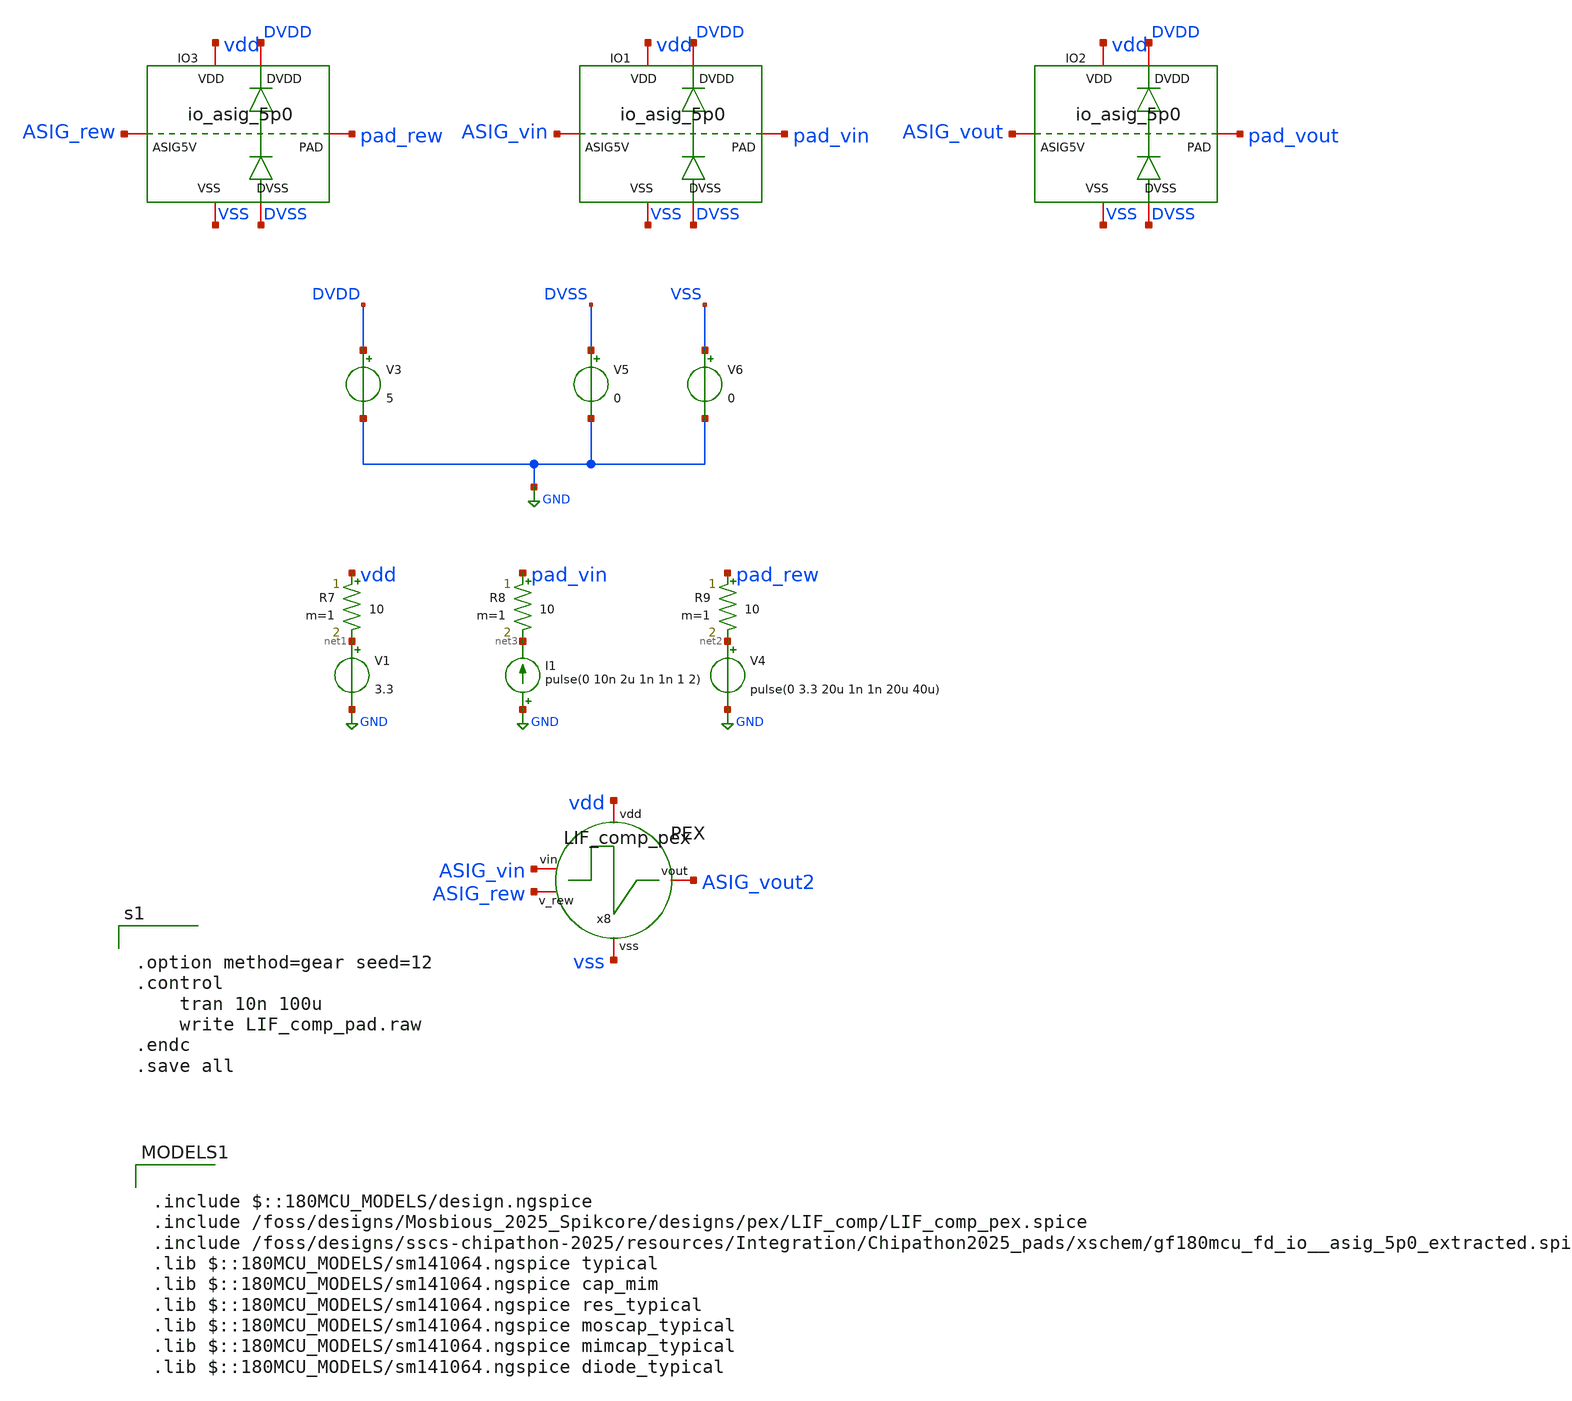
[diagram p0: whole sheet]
** sch_path: designs/pex_PADS/tb_LIF_comp/LIF_comp.sch
**.subckt LIF_comp
V1 net1 GND 3.3
V4 net2 GND pulse(0 3.3 20u 1n 1n 20u 40u)
x8 vdd vss ASIG_vin ASIG_rew ASIG_vout2 LIF_comp_pex
I1 GND net3 pulse(0 10n 2u 1n 1n 1 2)
R7 vdd net1 10 m=1
R8 pad_vin net3 10 m=1
R9 pad_rew net2 10 m=1
V3 DVDD GND 5
V5 DVSS GND 0
V6 VSS GND 0
XIO1 DVSS DVDD VSS vdd pad_vin ASIG_vin gf180mcu_fd_io__asig_5p0_extracted
XIO2 DVSS DVDD VSS vdd pad_vout ASIG_vout gf180mcu_fd_io__asig_5p0_extracted
XIO3 DVSS DVDD VSS vdd pad_rew ASIG_rew gf180mcu_fd_io__asig_5p0_extracted
**** begin user architecture code


.option method=gear seed=12
.control
    tran 10n 100u
    write LIF_comp_pad.raw
.endc
.save all



.include $::180MCU_MODELS/design.ngspice
.include /foss/designs/Mosbious_2025_Spikcore/designs/pex/LIF_comp/LIF_comp_pex.spice
.include /foss/designs/sscs-chipathon-2025/resources/Integration/Chipathon2025_pads/xschem/gf180mcu_fd_io__asig_5p0_extracted.spice
.lib $::180MCU_MODELS/sm141064.ngspice typical
.lib $::180MCU_MODELS/sm141064.ngspice cap_mim
.lib $::180MCU_MODELS/sm141064.ngspice res_typical
.lib $::180MCU_MODELS/sm141064.ngspice moscap_typical
.lib $::180MCU_MODELS/sm141064.ngspice mimcap_typical
.lib $::180MCU_MODELS/sm141064.ngspice diode_typical

**** end user architecture code
**.ends
.GLOBAL GND
.end
